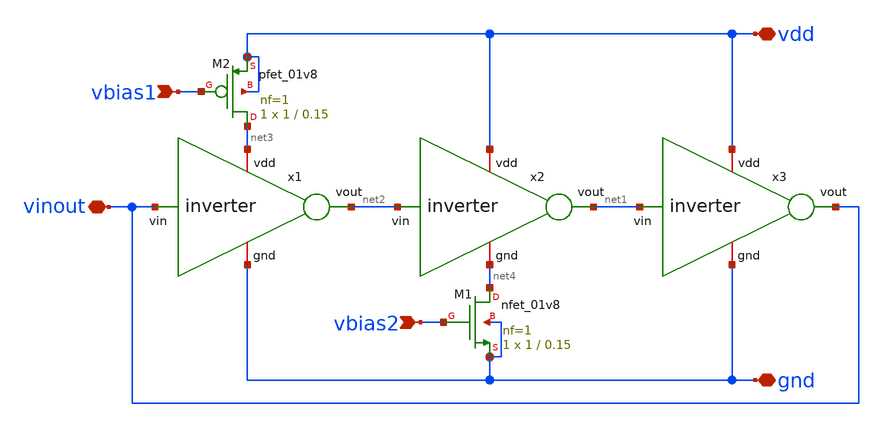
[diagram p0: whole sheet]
** sch_path: oscillator/oscillator.sch
**.subckt oscillator vdd gnd vbias2 vbias1 vinout
*.iopin vdd
*.iopin gnd
*.ipin vbias2
*.ipin vbias1
*.iopin vinout
x1 net3 net2 vinout gnd inverter
x2 vdd net1 net2 net4 inverter
x3 vdd vinout net1 gnd inverter
XM1 net4 vbias2 gnd gnd sky130_fd_pr__nfet_01v8 L=0.15 W=1 nf=1 ad='int((nf+1)/2) * W/nf * 0.29' as='int((nf+2)/2) * W/nf * 0.29'
+ pd='2*int((nf+1)/2) * (W/nf + 0.29)' ps='2*int((nf+2)/2) * (W/nf + 0.29)' nrd='0.29 / W' nrs='0.29 / W'
+ sa=0 sb=0 sd=0 mult=1 m=1
XM2 net3 vbias1 vdd vdd sky130_fd_pr__pfet_01v8 L=0.15 W=1 nf=1 ad='int((nf+1)/2) * W/nf * 0.29' as='int((nf+2)/2) * W/nf * 0.29'
+ pd='2*int((nf+1)/2) * (W/nf + 0.29)' ps='2*int((nf+2)/2) * (W/nf + 0.29)' nrd='0.29 / W' nrs='0.29 / W'
+ sa=0 sb=0 sd=0 mult=1 m=1
**.ends
.end
